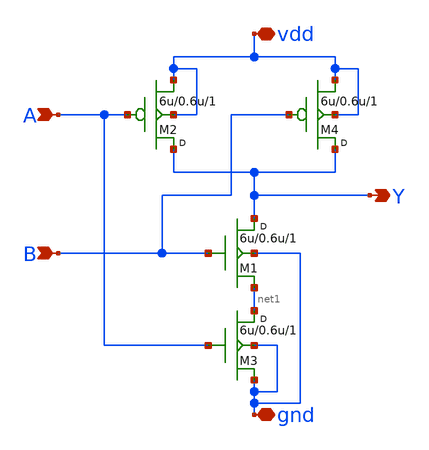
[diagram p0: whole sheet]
** sch_path: lab7/sch/nand.sch
**.subckt nand A B Y vdd gnd
*.ipin A
*.ipin B
*.opin Y
*.iopin vdd
*.iopin gnd
M3 net1 A gnd gnd nfet w=6u l=0.6u m=1
M4 Y B vdd vdd pfet w=6u l=0.6u m=1
M2 Y A vdd vdd pfet w=6u l=0.6u m=1
M1 Y B net1 gnd nfet w=6u l=0.6u m=1
**.ends
.end
